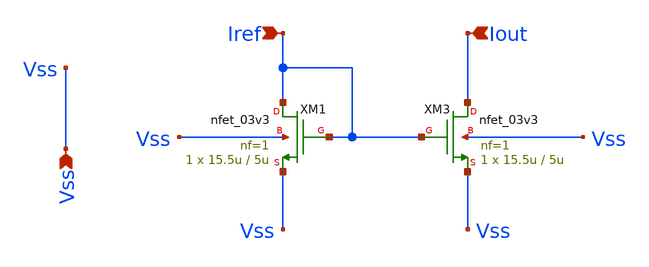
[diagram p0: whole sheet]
** sch_path: designs/libs/core_current-mirror/nmos_current_mirror/nmos_current_mirror.sch
**.subckt nmos_current_mirror Vss Iref Iout
*.ipin Vss
*.ipin Iref
*.ipin Iout
XM1 Iref Iref Vss Vss nfet_03v3 L=5u W=15.5u nf=1 ad='int((nf+1)/2) * W/nf * 0.18u' as='int((nf+2)/2) * W/nf * 0.18u'
+ pd='2*int((nf+1)/2) * (W/nf + 0.18u)' ps='2*int((nf+2)/2) * (W/nf + 0.18u)' nrd='0.18u / W' nrs='0.18u / W'
+ sa=0 sb=0 sd=0 m=1
XM3 Iout Iref Vss Vss nfet_03v3 L=5u W=15.5u nf=1 ad='int((nf+1)/2) * W/nf * 0.18u' as='int((nf+2)/2) * W/nf * 0.18u'
+ pd='2*int((nf+1)/2) * (W/nf + 0.18u)' ps='2*int((nf+2)/2) * (W/nf + 0.18u)' nrd='0.18u / W' nrs='0.18u / W'
+ sa=0 sb=0 sd=0 m=1
**.ends
.end
